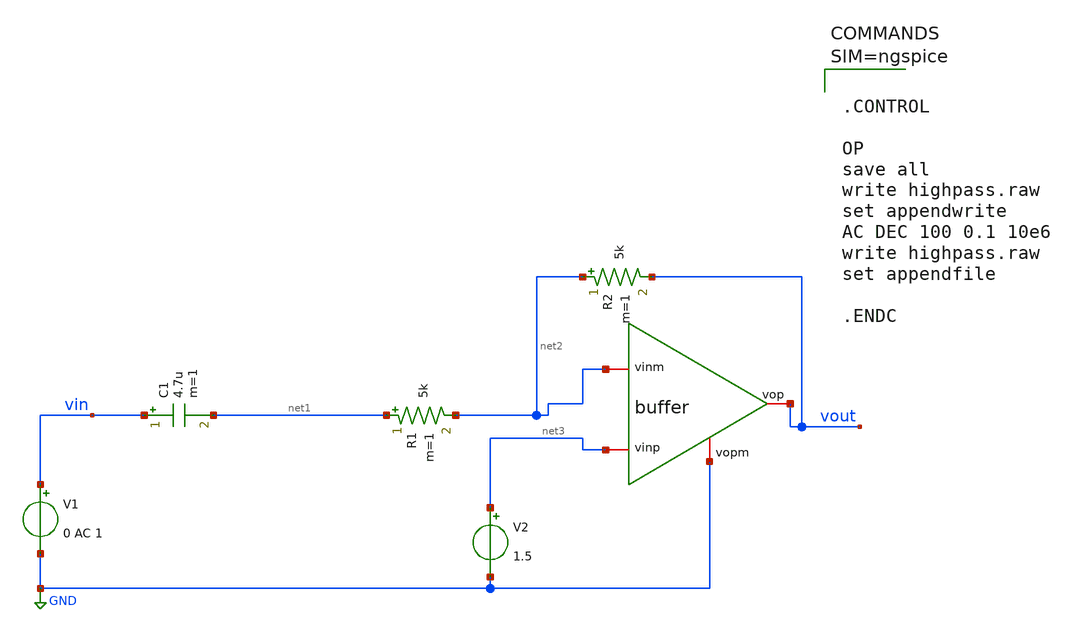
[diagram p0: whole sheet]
** sch_path: work/xschem/highpass.sch
**.subckt highpass
V1 vin GND 0 AC 1
C1 vin net1 4.7u m=1
R1 net1 net2 5k m=1
R2 net2 vout 5k m=1
V2 net3 GND 1.5
x1 vout net3 net2 GND buffer
**** begin user architecture code



.CONTROL

OP
save all
write highpass.raw
set appendwrite
AC DEC 100 0.1 10e6
write highpass.raw
set appendfile

.ENDC



**** end user architecture code
**.ends

* expanding   symbol:  buffer.sym # of pins=4
** sym_path: work/xschem/buffer.sym
** sch_path: work/xschem/buffer.sch
.subckt buffer vop vinp vinm vopm
*.iopin vinp
*.iopin vinm
*.iopin vop
*.iopin vopm
E1 vop vopm net1 GND 1
E2 net2 GND vinp vinm 1000
R1 net2 net1 15.9k m=1
C1 net1 GND 10n m=1
.ends

.GLOBAL GND
.end
